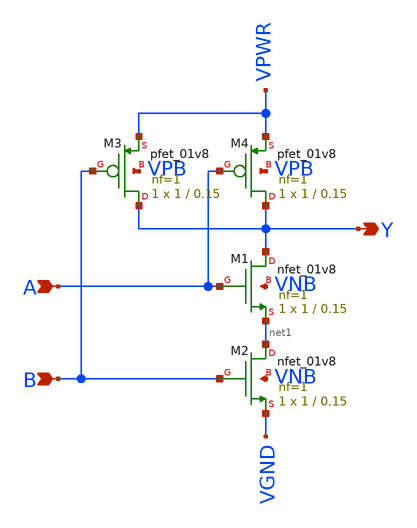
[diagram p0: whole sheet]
** sch_path: xschem/rowdec_nand2.sch
**.subckt rowdec_nand2 A Y B
*.ipin A
*.opin Y
*.ipin B
XM1 Y A net1 VNB sky130_fd_pr__nfet_01v8 L=0.15 W=1 nf=1 ad='int((nf+1)/2) * W/nf * 0.29' as='int((nf+2)/2) * W/nf * 0.29'
+ pd='2*int((nf+1)/2) * (W/nf + 0.29)' ps='2*int((nf+2)/2) * (W/nf + 0.29)' nrd='0.29 / W' nrs='0.29 / W'
+ sa=0 sb=0 sd=0 mult=1 m=1
XM3 Y B VPWR VPB sky130_fd_pr__pfet_01v8 L=0.15 W=1 nf=1 ad='int((nf+1)/2) * W/nf * 0.29' as='int((nf+2)/2) * W/nf * 0.29'
+ pd='2*int((nf+1)/2) * (W/nf + 0.29)' ps='2*int((nf+2)/2) * (W/nf + 0.29)' nrd='0.29 / W' nrs='0.29 / W'
+ sa=0 sb=0 sd=0 mult=1 m=1
XM2 net1 B VGND VNB sky130_fd_pr__nfet_01v8 L=0.15 W=1 nf=1 ad='int((nf+1)/2) * W/nf * 0.29' as='int((nf+2)/2) * W/nf * 0.29'
+ pd='2*int((nf+1)/2) * (W/nf + 0.29)' ps='2*int((nf+2)/2) * (W/nf + 0.29)' nrd='0.29 / W' nrs='0.29 / W'
+ sa=0 sb=0 sd=0 mult=1 m=1
XM4 Y A VPWR VPB sky130_fd_pr__pfet_01v8 L=0.15 W=1 nf=1 ad='int((nf+1)/2) * W/nf * 0.29' as='int((nf+2)/2) * W/nf * 0.29'
+ pd='2*int((nf+1)/2) * (W/nf + 0.29)' ps='2*int((nf+2)/2) * (W/nf + 0.29)' nrd='0.29 / W' nrs='0.29 / W'
+ sa=0 sb=0 sd=0 mult=1 m=1
**.ends
.end
